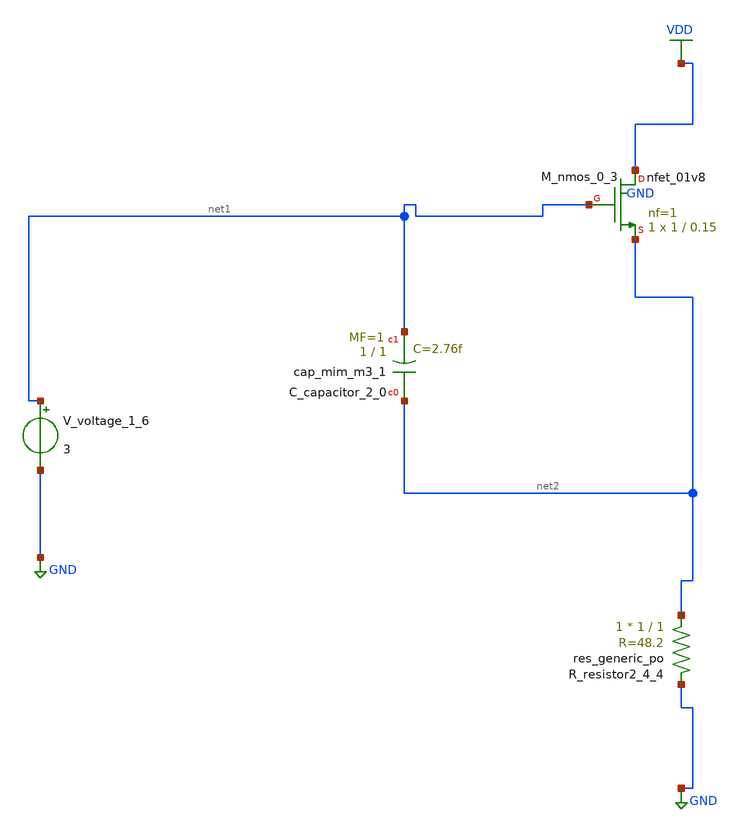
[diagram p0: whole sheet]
** sch_path: schematics/AMSNet/371.sch
**.subckt 371
XC_capacitor_2_0 net2 net1 sky130_fd_pr__cap_mim_m3_1 W=1 L=1 MF=1 m=1
XM_nmos_0_3 VDD net1 net2 GND sky130_fd_pr__nfet_01v8 L=0.15 W=1 nf=1 ad='int((1 + 1)/2) * 1 / 1 * 0.29'
+ as='int((1 + 2)/2) * 1 / 1 * 0.29' pd='2*int((1 + 1)/2) * (1 / 1 + 0.29)' ps='2*int((1 + 2)/2) * (1 / 1 + 0.29)'
+ nrd='0.29 / 1 ' nrs='0.29 / 1 ' sa=0 sb=0 sd=0 mult=1 m=1
XR_resistor2_4_4 net2 GND sky130_fd_pr__res_generic_po W=1 L=1 m=1
V_voltage_1_6 net1 GND 3
**.ends
.GLOBAL GND
.GLOBAL VDD
.end
